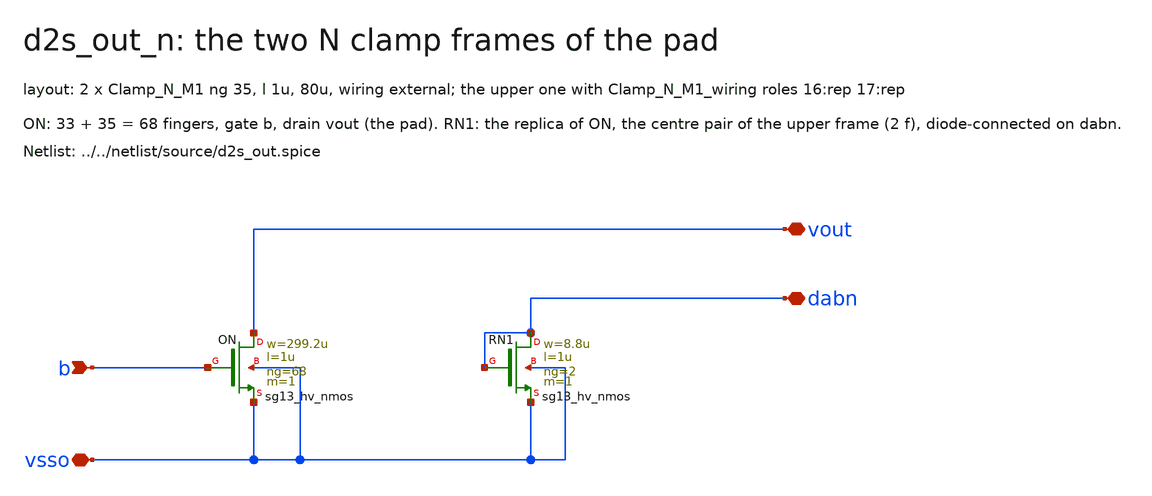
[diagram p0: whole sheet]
** sch_path: macros/sg13cmos5l_IOPadDiff2Single/schematic/xschem/d2s_out_n.sch
**.subckt d2s_out_n vsso b vout dabn
*.iopin vsso
*.ipin b
*.iopin vout
*.iopin dabn
XON vout b vsso vsso sg13_hv_nmos w=299.2u l=1u ng=68 m=1 mm_ok=1
XRN1 dabn dabn vsso vsso sg13_hv_nmos w=8.8u l=1u ng=2 m=1 mm_ok=1
**.ends
.end
